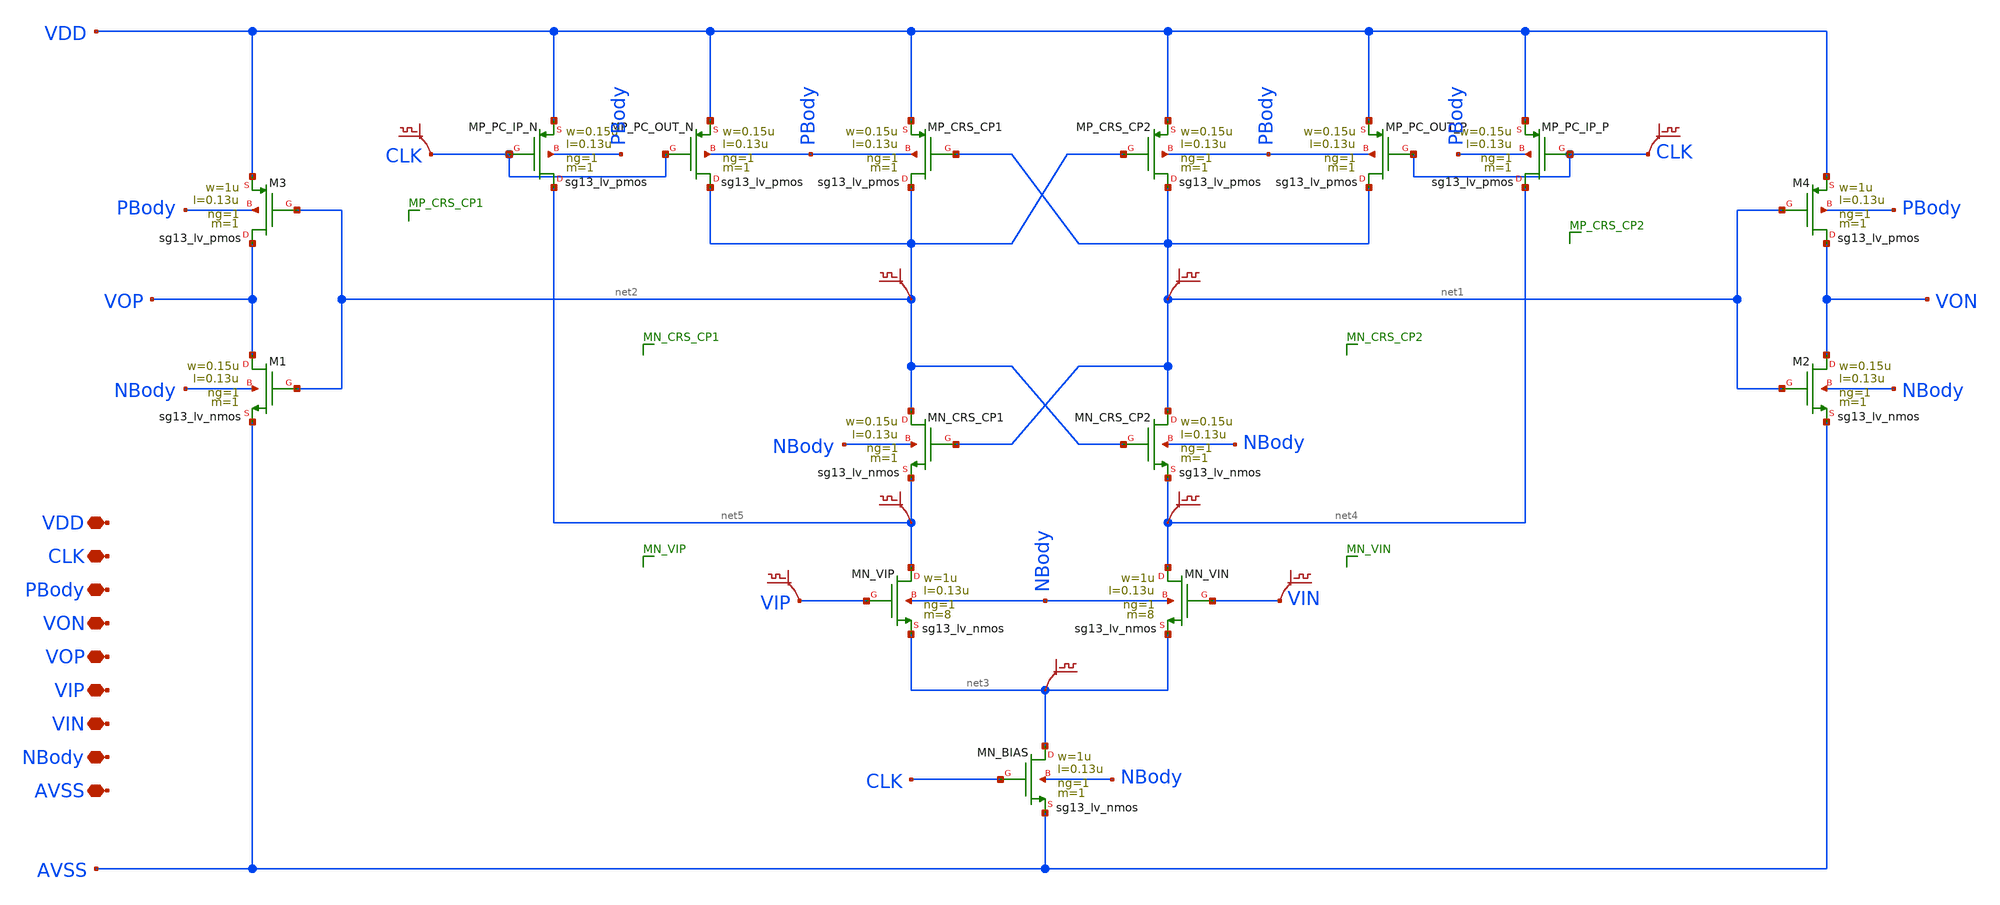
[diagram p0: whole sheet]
** sch_path: COMP/COMP_NMOS_IP.sch
**.subckt COMP_NMOS_IP VDD CLK PBody VON VOP VIP VIN NBody AVSS
*.iopin VDD
*.iopin CLK
*.iopin PBody
*.iopin VON
*.iopin VOP
*.iopin VIP
*.iopin VIN
*.iopin NBody
*.iopin AVSS
XMN_VIP net5 VIP net3 NBody sg13_lv_nmos w=1u l=0.13u ng=1 m=8 mm_ok=1
XMN_VIN net4 VIN net3 NBody sg13_lv_nmos w=1u l=0.13u ng=1 m=8 mm_ok=1
XMP_CRS_CP2 net1 net2 VDD PBody sg13_lv_pmos w=0.15u l=0.13u ng=1 m=1 mm_ok=1
XMP_CRS_CP1 net2 net1 VDD PBody sg13_lv_pmos w=0.15u l=0.13u ng=1 m=1 mm_ok=1
XMN_CRS_CP1 net2 net1 net5 NBody sg13_lv_nmos w=0.15u l=0.13u ng=1 m=1 mm_ok=1
XMN_CRS_CP2 net1 net2 net4 NBody sg13_lv_nmos w=0.15u l=0.13u ng=1 m=1 mm_ok=1
XMP_PC_OUT_P net1 CLK VDD PBody sg13_lv_pmos w=0.15u l=0.13u ng=1 m=1 mm_ok=1
XMP_PC_IP_P net4 CLK VDD PBody sg13_lv_pmos w=0.15u l=0.13u ng=1 m=1 mm_ok=1
XMP_PC_OUT_N net2 CLK VDD PBody sg13_lv_pmos w=0.15u l=0.13u ng=1 m=1 mm_ok=1
XMP_PC_IP_N net5 CLK VDD PBody sg13_lv_pmos w=0.15u l=0.13u ng=1 m=1 mm_ok=1
XMN_BIAS net3 CLK AVSS NBody sg13_lv_nmos w=1u l=0.13u ng=1 m=1 mm_ok=1
.save v(net1)
.save v(net2)
.save v(net4)
.save v(net3)
.save v(vin)
.save v(vip)
.save v(clk)
XM1 VOP net2 AVSS NBody sg13_lv_nmos w=0.15u l=0.13u ng=1 m=1 mm_ok=1
XM3 VOP net2 VDD PBody sg13_lv_pmos w=1u l=0.13u ng=1 m=1 mm_ok=1
XM2 VON net1 AVSS NBody sg13_lv_nmos w=0.15u l=0.13u ng=1 m=1 mm_ok=1
XM4 VON net1 VDD PBody sg13_lv_pmos w=1u l=0.13u ng=1 m=1 mm_ok=1
.save v(net5)
.save v(clk)
**.ends
.end
